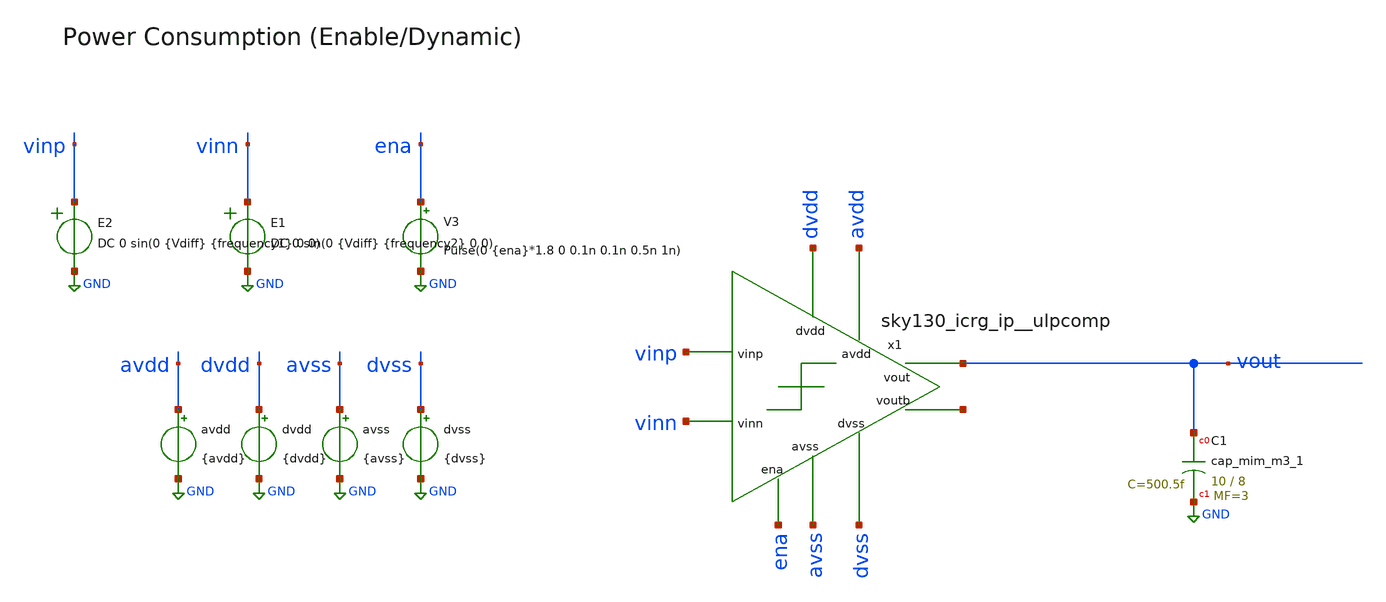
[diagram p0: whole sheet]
** sch_path: cace/tb_dynamic_current.sch
**.subckt tb_dynamic_current
V3 ena GND Pulse(0 {ena}*1.8 0 0.1n 0.1n 0.5n 1n)
avdd avdd GND {avdd}
dvdd dvdd GND {dvdd}
avss avss GND {avss}
dvss dvss GND {dvss}
E1 vinn GND VOL=' DC 0 sin(0 {Vdiff} {frequency2} 0 0) '
E2 vinp GND VOL=' DC 0 sin(0 {Vdiff} {frequency1} 0 0) '
XC1 vout GND sky130_fd_pr__cap_mim_m3_1 W=10 L=8 MF=3 m=3
x1 dvdd avdd ena vinp vinn vout net1 avss dvss sky130_icrg_ip__ulpcomp
**** begin user architecture code


.lib /home/ttuser/pdk/sky130A/libs.tech/combined/sky130.lib.spice {corner}
.option TEMP={temperature}


.control
tran [1.0 / {frequency1} / 100] [1 / {frequency1}]
set wr_singlescale
wrdata {simpath}/{filename}_{N}.data -I(dvdd)
quit
.endc

**** end user architecture code
**.ends
.GLOBAL GND
.end
